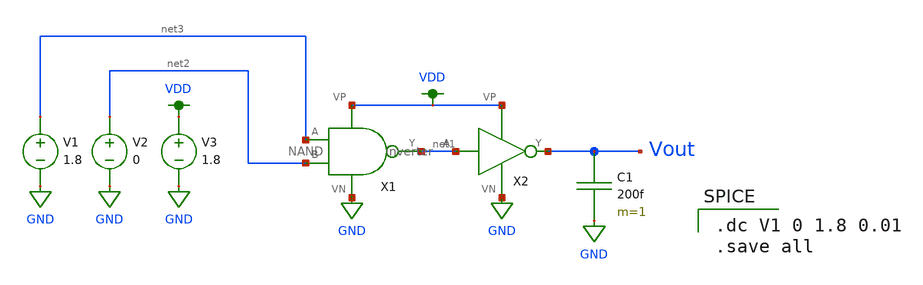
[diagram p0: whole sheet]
** sch_path: Miniproject1/AND_transient.sch
**.subckt AND_transient
X2 net1 Vout VDD GND inverter
V1 net3 GND 1.8
V2 net2 GND 0
V3 VDD GND 1.8
C1 Vout GND 200f m=1
X1 net3 net2 net1 VDD GND NAND
**** begin user architecture code

.option wnflag=1
.lib ~/skywater/skywater-pdk/libraries/sky130_fd_pr_ngspice/latest/models/sky130.lib.spice tt


.dc V1 0 1.8 0.01
.save all

**** end user architecture code
**.ends

* expanding   symbol:  /home/james/Documents/Miniproject1/inverter.sym # of pins=4
** sym_path: Miniproject1/inverter.sym
** sch_path: Miniproject1/inverter.sch
.subckt inverter A Y VP VN
*.ipin A
*.iopin VP
*.iopin VN
*.opin Y
XM2 Y A VP VDD sky130_fd_pr__pfet_01v8 L=0.15 W=1 nf=1 ad='int((nf+1)/2) * W/nf * 0.29' as='int((nf+2)/2) * W/nf * 0.29'
+ pd='2*int((nf+1)/2) * (W/nf + 0.29)' ps='2*int((nf+2)/2) * (W/nf + 0.29)' nrd='0.29 / W' nrs='0.29 / W'
+ sa=0 sb=0 sd=0 mult=1 m=1
XM1 Y A VN GND sky130_fd_pr__nfet_01v8 L=0.15 W=1 nf=1 ad='int((nf+1)/2) * W/nf * 0.29' as='int((nf+2)/2) * W/nf * 0.29'
+ pd='2*int((nf+1)/2) * (W/nf + 0.29)' ps='2*int((nf+2)/2) * (W/nf + 0.29)' nrd='0.29 / W' nrs='0.29 / W'
+ sa=0 sb=0 sd=0 mult=1 m=1
.ends


* expanding   symbol:  /home/james/Documents/Miniproject1/NAND.sym # of pins=5
** sym_path: Miniproject1/NAND.sym
** sch_path: Miniproject1/NAND.sch
.subckt NAND A B Y VP VN
*.opin Y
*.ipin A
*.ipin B
*.iopin VP
*.iopin VN
XM1 VP B Y VDD sky130_fd_pr__pfet_01v8 L=0.15 W=1 nf=1 ad='int((nf+1)/2) * W/nf * 0.29' as='int((nf+2)/2) * W/nf * 0.29'
+ pd='2*int((nf+1)/2) * (W/nf + 0.29)' ps='2*int((nf+2)/2) * (W/nf + 0.29)' nrd='0.29 / W' nrs='0.29 / W'
+ sa=0 sb=0 sd=0 mult=1 m=1
XM2 Y A VP VDD sky130_fd_pr__pfet_01v8 L=0.15 W=1 nf=1 ad='int((nf+1)/2) * W/nf * 0.29' as='int((nf+2)/2) * W/nf * 0.29'
+ pd='2*int((nf+1)/2) * (W/nf + 0.29)' ps='2*int((nf+2)/2) * (W/nf + 0.29)' nrd='0.29 / W' nrs='0.29 / W'
+ sa=0 sb=0 sd=0 mult=1 m=1
XM3 Y A net1 GND sky130_fd_pr__nfet_01v8 L=0.15 W=1 nf=1 ad='int((nf+1)/2) * W/nf * 0.29' as='int((nf+2)/2) * W/nf * 0.29'
+ pd='2*int((nf+1)/2) * (W/nf + 0.29)' ps='2*int((nf+2)/2) * (W/nf + 0.29)' nrd='0.29 / W' nrs='0.29 / W'
+ sa=0 sb=0 sd=0 mult=1 m=1
XM4 VN B net1 GND sky130_fd_pr__nfet_01v8 L=0.15 W=1 nf=1 ad='int((nf+1)/2) * W/nf * 0.29' as='int((nf+2)/2) * W/nf * 0.29'
+ pd='2*int((nf+1)/2) * (W/nf + 0.29)' ps='2*int((nf+2)/2) * (W/nf + 0.29)' nrd='0.29 / W' nrs='0.29 / W'
+ sa=0 sb=0 sd=0 mult=1 m=1
.ends

.GLOBAL VDD
.GLOBAL GND
.end
